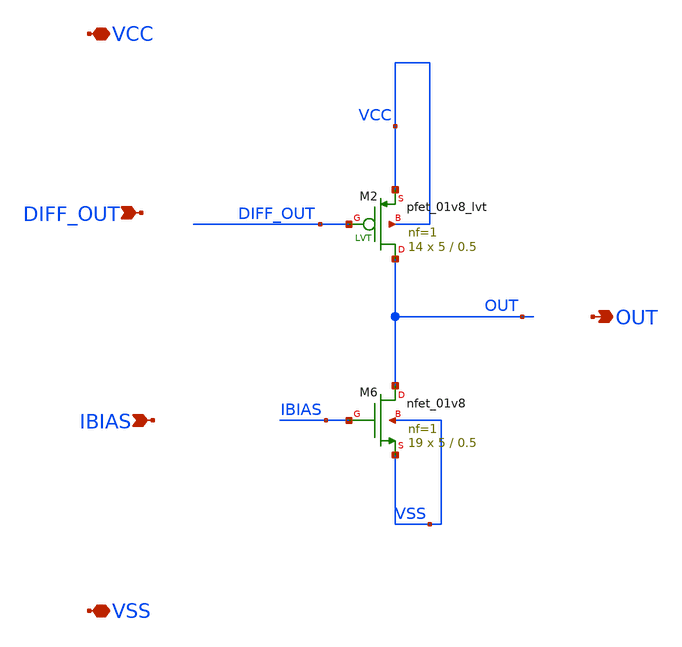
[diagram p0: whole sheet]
** sch_path: xschem/second_stage.sch
**.subckt second_stage VCC VSS IBIAS DIFF_OUT OUT
*.iopin VCC
*.iopin VSS
*.ipin IBIAS
*.ipin DIFF_OUT
*.opin OUT
XM6 OUT IBIAS VSS VSS sky130_fd_pr__nfet_01v8 L=0.5 W=5 nf=1 ad='int((nf+1)/2) * W/nf * 0.29' as='int((nf+2)/2) * W/nf * 0.29'
+ pd='2*int((nf+1)/2) * (W/nf + 0.29)' ps='2*int((nf+2)/2) * (W/nf + 0.29)' nrd='0.29 / W' nrs='0.29 / W'
+ sa=0 sb=0 sd=0 mult=19 m=19
XM2 OUT DIFF_OUT VCC VCC sky130_fd_pr__pfet_01v8_lvt L=0.5 W=5 nf=1 ad='int((nf+1)/2) * W/nf * 0.29'
+ as='int((nf+2)/2) * W/nf * 0.29' pd='2*int((nf+1)/2) * (W/nf + 0.29)' ps='2*int((nf+2)/2) * (W/nf + 0.29)'
+ nrd='0.29 / W' nrs='0.29 / W' sa=0 sb=0 sd=0 mult=14 m=14
**.ends
.end
